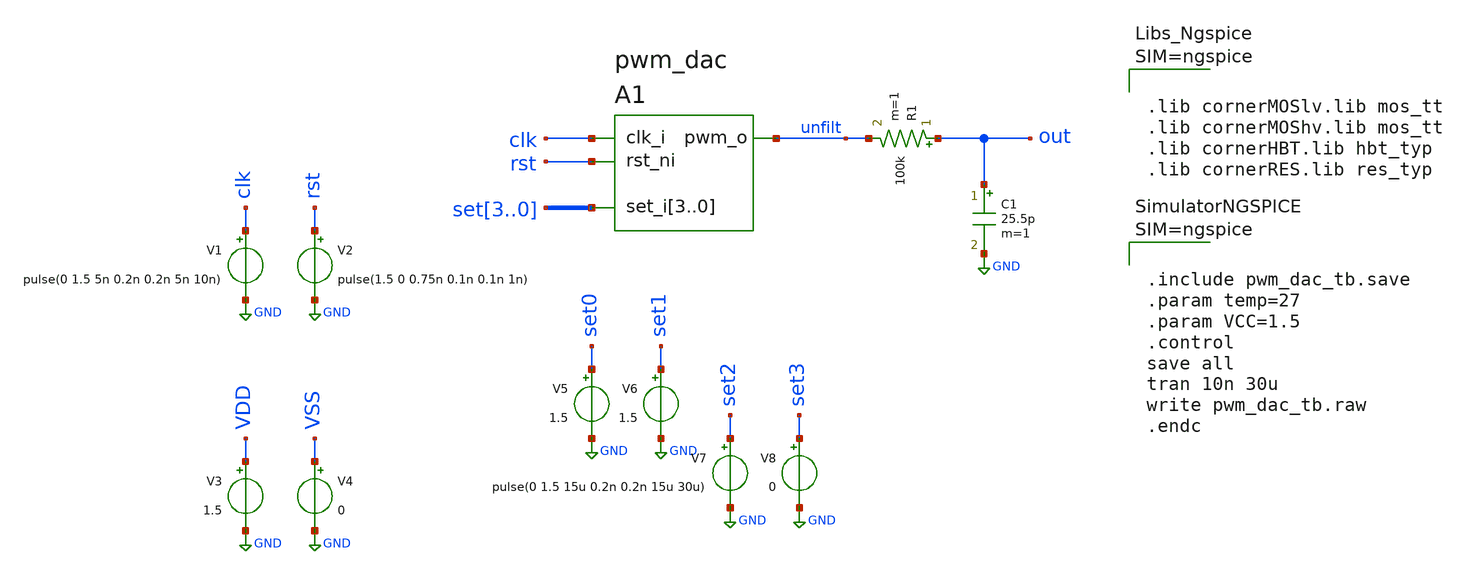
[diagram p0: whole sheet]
** sch_path: cosim/pwm_dac_tb.sch
**.subckt pwm_dac_tb
R1 out unfilt 100k m=1
C1 out GND 25.5p m=1
A1 [ clk rst set3 set2 set1 set0 ] [ unfilt ] pwm_dac
V1 clk GND pulse(0 1.5 5n 0.2n 0.2n 5n 10n)
V2 rst GND pulse(1.5 0 0.75n 0.1n 0.1n 1n)
V3 VDD GND 1.5
V4 VSS GND 0
V5 set0 GND 1.5
V6 set1 GND 1.5
V7 set2 GND pulse(0 1.5 15u 0.2n 0.2n 15u 30u)
V8 set3 GND 0
**** begin user architecture code



.lib cornerMOSlv.lib mos_tt
.lib cornerMOShv.lib mos_tt
.lib cornerHBT.lib hbt_typ
.lib cornerRES.lib res_typ






.include pwm_dac_tb.save
.param temp=27
.param VCC=1.5
.control
save all
tran 10n 30u
write pwm_dac_tb.raw
.endc



**** end user architecture code
**.ends
.GLOBAL GND
**** begin user architecture code
.model pwm_dac d_cosim simulation="ivlng" sim_args=["../pwm_dac"]
**** end user architecture code
.end
